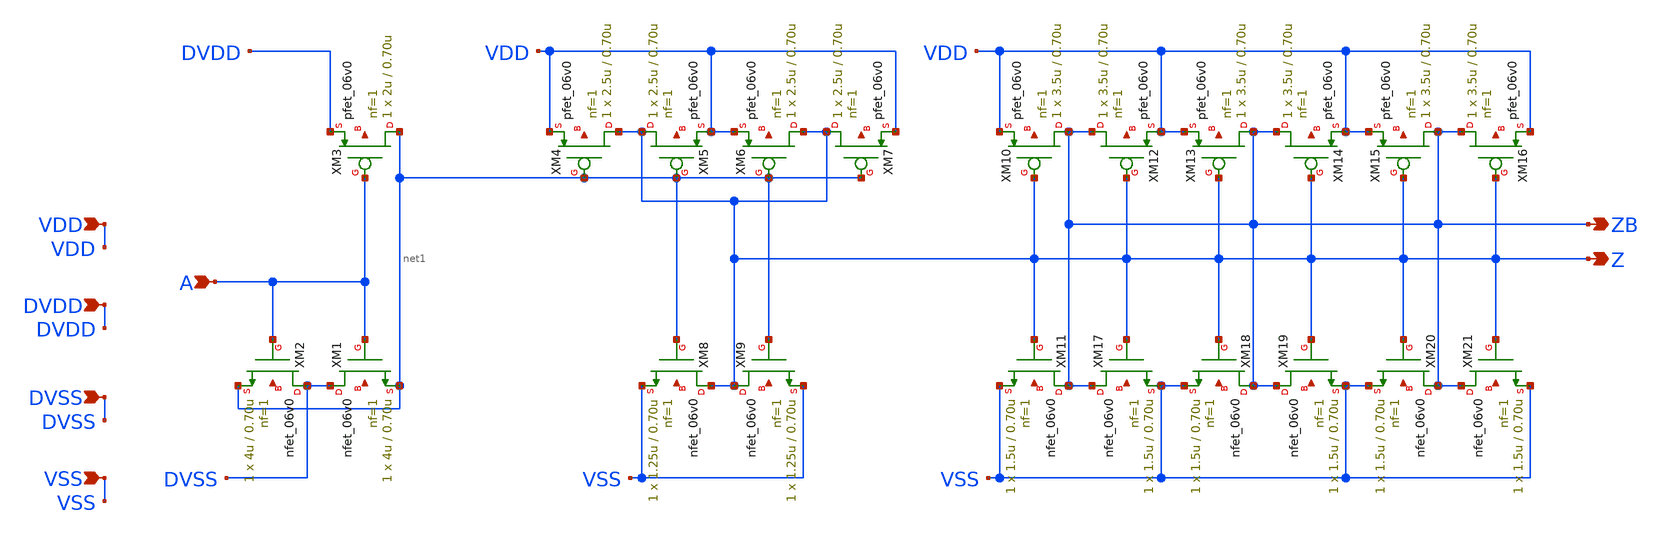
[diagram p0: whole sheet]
** sch_path: gf180mcu_fd_io__bi_24t/comp018green_in_drv.sch
**.subckt comp018green_in_drv A DVDD DVSS Z ZB VDD VSS
*.ipin A
*.ipin DVDD
*.ipin DVSS
*.opin Z
*.opin ZB
*.ipin VDD
*.ipin VSS
XM1 DVSS A net1 net2 nfet_06v0 L=0.70u W=4u nf=1 ad='int((nf+1)/2) * W/nf * 0.18u' as='int((nf+2)/2) * W/nf * 0.18u'
+ pd='2*int((nf+1)/2) * (W/nf + 0.18u)' ps='2*int((nf+2)/2) * (W/nf + 0.18u)' nrd='0.18u / W' nrs='0.18u / W'
+ sa=0 sb=0 sd=0 m=1
XM3 net1 A DVDD net3 pfet_06v0 L=0.70u W=2u nf=1 ad='int((nf+1)/2) * W/nf * 0.18u' as='int((nf+2)/2) * W/nf * 0.18u'
+ pd='2*int((nf+1)/2) * (W/nf + 0.18u)' ps='2*int((nf+2)/2) * (W/nf + 0.18u)' nrd='0.18u / W' nrs='0.18u / W'
+ sa=0 sb=0 sd=0 m=1
XM2 DVSS A net1 net4 nfet_06v0 L=0.70u W=4u nf=1 ad='int((nf+1)/2) * W/nf * 0.18u' as='int((nf+2)/2) * W/nf * 0.18u'
+ pd='2*int((nf+1)/2) * (W/nf + 0.18u)' ps='2*int((nf+2)/2) * (W/nf + 0.18u)' nrd='0.18u / W' nrs='0.18u / W'
+ sa=0 sb=0 sd=0 m=1
XM4 Z net1 VDD net5 pfet_06v0 L=0.70u W=2.5u nf=1 ad='int((nf+1)/2) * W/nf * 0.18u' as='int((nf+2)/2) * W/nf * 0.18u'
+ pd='2*int((nf+1)/2) * (W/nf + 0.18u)' ps='2*int((nf+2)/2) * (W/nf + 0.18u)' nrd='0.18u / W' nrs='0.18u / W'
+ sa=0 sb=0 sd=0 m=1
XM5 Z net1 VDD net6 pfet_06v0 L=0.70u W=2.5u nf=1 ad='int((nf+1)/2) * W/nf * 0.18u' as='int((nf+2)/2) * W/nf * 0.18u'
+ pd='2*int((nf+1)/2) * (W/nf + 0.18u)' ps='2*int((nf+2)/2) * (W/nf + 0.18u)' nrd='0.18u / W' nrs='0.18u / W'
+ sa=0 sb=0 sd=0 m=1
XM6 Z net1 VDD net7 pfet_06v0 L=0.70u W=2.5u nf=1 ad='int((nf+1)/2) * W/nf * 0.18u' as='int((nf+2)/2) * W/nf * 0.18u'
+ pd='2*int((nf+1)/2) * (W/nf + 0.18u)' ps='2*int((nf+2)/2) * (W/nf + 0.18u)' nrd='0.18u / W' nrs='0.18u / W'
+ sa=0 sb=0 sd=0 m=1
XM7 Z net1 VDD net8 pfet_06v0 L=0.70u W=2.5u nf=1 ad='int((nf+1)/2) * W/nf * 0.18u' as='int((nf+2)/2) * W/nf * 0.18u'
+ pd='2*int((nf+1)/2) * (W/nf + 0.18u)' ps='2*int((nf+2)/2) * (W/nf + 0.18u)' nrd='0.18u / W' nrs='0.18u / W'
+ sa=0 sb=0 sd=0 m=1
XM8 Z net1 VSS net9 nfet_06v0 L=0.70u W=1.25u nf=1 ad='int((nf+1)/2) * W/nf * 0.18u' as='int((nf+2)/2) * W/nf * 0.18u'
+ pd='2*int((nf+1)/2) * (W/nf + 0.18u)' ps='2*int((nf+2)/2) * (W/nf + 0.18u)' nrd='0.18u / W' nrs='0.18u / W'
+ sa=0 sb=0 sd=0 m=1
XM9 Z net1 VSS net10 nfet_06v0 L=0.70u W=1.25u nf=1 ad='int((nf+1)/2) * W/nf * 0.18u' as='int((nf+2)/2) * W/nf * 0.18u'
+ pd='2*int((nf+1)/2) * (W/nf + 0.18u)' ps='2*int((nf+2)/2) * (W/nf + 0.18u)' nrd='0.18u / W' nrs='0.18u / W'
+ sa=0 sb=0 sd=0 m=1
XM10 ZB Z VDD net11 pfet_06v0 L=0.70u W=3.5u nf=1 ad='int((nf+1)/2) * W/nf * 0.18u' as='int((nf+2)/2) * W/nf * 0.18u'
+ pd='2*int((nf+1)/2) * (W/nf + 0.18u)' ps='2*int((nf+2)/2) * (W/nf + 0.18u)' nrd='0.18u / W' nrs='0.18u / W'
+ sa=0 sb=0 sd=0 m=1
XM11 ZB Z VSS net12 nfet_06v0 L=0.70u W=1.5u nf=1 ad='int((nf+1)/2) * W/nf * 0.18u' as='int((nf+2)/2) * W/nf * 0.18u'
+ pd='2*int((nf+1)/2) * (W/nf + 0.18u)' ps='2*int((nf+2)/2) * (W/nf + 0.18u)' nrd='0.18u / W' nrs='0.18u / W'
+ sa=0 sb=0 sd=0 m=1
XM12 ZB Z VDD net13 pfet_06v0 L=0.70u W=3.5u nf=1 ad='int((nf+1)/2) * W/nf * 0.18u' as='int((nf+2)/2) * W/nf * 0.18u'
+ pd='2*int((nf+1)/2) * (W/nf + 0.18u)' ps='2*int((nf+2)/2) * (W/nf + 0.18u)' nrd='0.18u / W' nrs='0.18u / W'
+ sa=0 sb=0 sd=0 m=1
XM13 ZB Z VDD net14 pfet_06v0 L=0.70u W=3.5u nf=1 ad='int((nf+1)/2) * W/nf * 0.18u' as='int((nf+2)/2) * W/nf * 0.18u'
+ pd='2*int((nf+1)/2) * (W/nf + 0.18u)' ps='2*int((nf+2)/2) * (W/nf + 0.18u)' nrd='0.18u / W' nrs='0.18u / W'
+ sa=0 sb=0 sd=0 m=1
XM14 ZB Z VDD net15 pfet_06v0 L=0.70u W=3.5u nf=1 ad='int((nf+1)/2) * W/nf * 0.18u' as='int((nf+2)/2) * W/nf * 0.18u'
+ pd='2*int((nf+1)/2) * (W/nf + 0.18u)' ps='2*int((nf+2)/2) * (W/nf + 0.18u)' nrd='0.18u / W' nrs='0.18u / W'
+ sa=0 sb=0 sd=0 m=1
XM15 ZB Z VDD net16 pfet_06v0 L=0.70u W=3.5u nf=1 ad='int((nf+1)/2) * W/nf * 0.18u' as='int((nf+2)/2) * W/nf * 0.18u'
+ pd='2*int((nf+1)/2) * (W/nf + 0.18u)' ps='2*int((nf+2)/2) * (W/nf + 0.18u)' nrd='0.18u / W' nrs='0.18u / W'
+ sa=0 sb=0 sd=0 m=1
XM16 ZB Z VDD net17 pfet_06v0 L=0.70u W=3.5u nf=1 ad='int((nf+1)/2) * W/nf * 0.18u' as='int((nf+2)/2) * W/nf * 0.18u'
+ pd='2*int((nf+1)/2) * (W/nf + 0.18u)' ps='2*int((nf+2)/2) * (W/nf + 0.18u)' nrd='0.18u / W' nrs='0.18u / W'
+ sa=0 sb=0 sd=0 m=1
XM17 ZB Z VSS net18 nfet_06v0 L=0.70u W=1.5u nf=1 ad='int((nf+1)/2) * W/nf * 0.18u' as='int((nf+2)/2) * W/nf * 0.18u'
+ pd='2*int((nf+1)/2) * (W/nf + 0.18u)' ps='2*int((nf+2)/2) * (W/nf + 0.18u)' nrd='0.18u / W' nrs='0.18u / W'
+ sa=0 sb=0 sd=0 m=1
XM18 ZB Z VSS net19 nfet_06v0 L=0.70u W=1.5u nf=1 ad='int((nf+1)/2) * W/nf * 0.18u' as='int((nf+2)/2) * W/nf * 0.18u'
+ pd='2*int((nf+1)/2) * (W/nf + 0.18u)' ps='2*int((nf+2)/2) * (W/nf + 0.18u)' nrd='0.18u / W' nrs='0.18u / W'
+ sa=0 sb=0 sd=0 m=1
XM19 ZB Z VSS net20 nfet_06v0 L=0.70u W=1.5u nf=1 ad='int((nf+1)/2) * W/nf * 0.18u' as='int((nf+2)/2) * W/nf * 0.18u'
+ pd='2*int((nf+1)/2) * (W/nf + 0.18u)' ps='2*int((nf+2)/2) * (W/nf + 0.18u)' nrd='0.18u / W' nrs='0.18u / W'
+ sa=0 sb=0 sd=0 m=1
XM20 ZB Z VSS net21 nfet_06v0 L=0.70u W=1.5u nf=1 ad='int((nf+1)/2) * W/nf * 0.18u' as='int((nf+2)/2) * W/nf * 0.18u'
+ pd='2*int((nf+1)/2) * (W/nf + 0.18u)' ps='2*int((nf+2)/2) * (W/nf + 0.18u)' nrd='0.18u / W' nrs='0.18u / W'
+ sa=0 sb=0 sd=0 m=1
XM21 ZB Z VSS net22 nfet_06v0 L=0.70u W=1.5u nf=1 ad='int((nf+1)/2) * W/nf * 0.18u' as='int((nf+2)/2) * W/nf * 0.18u'
+ pd='2*int((nf+1)/2) * (W/nf + 0.18u)' ps='2*int((nf+2)/2) * (W/nf + 0.18u)' nrd='0.18u / W' nrs='0.18u / W'
+ sa=0 sb=0 sd=0 m=1
**.ends
.end
